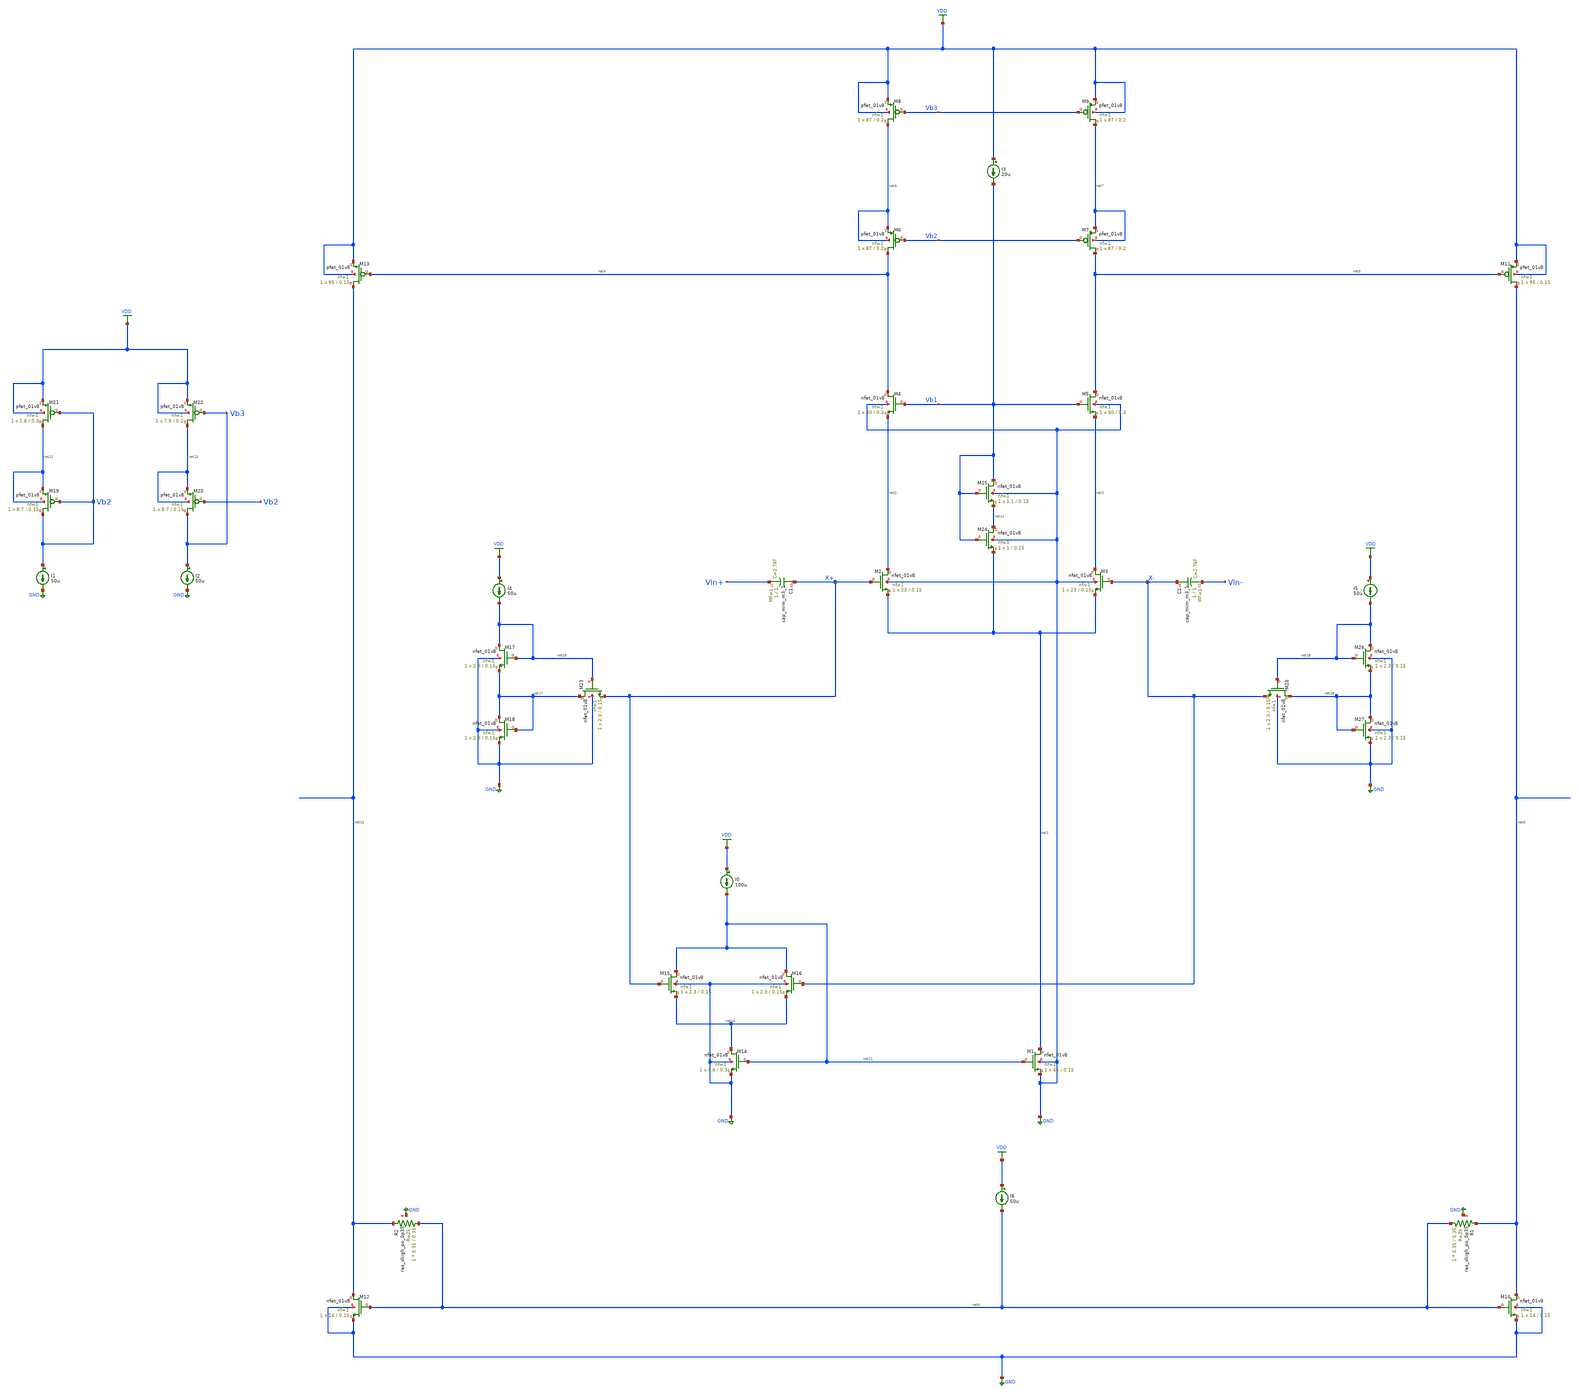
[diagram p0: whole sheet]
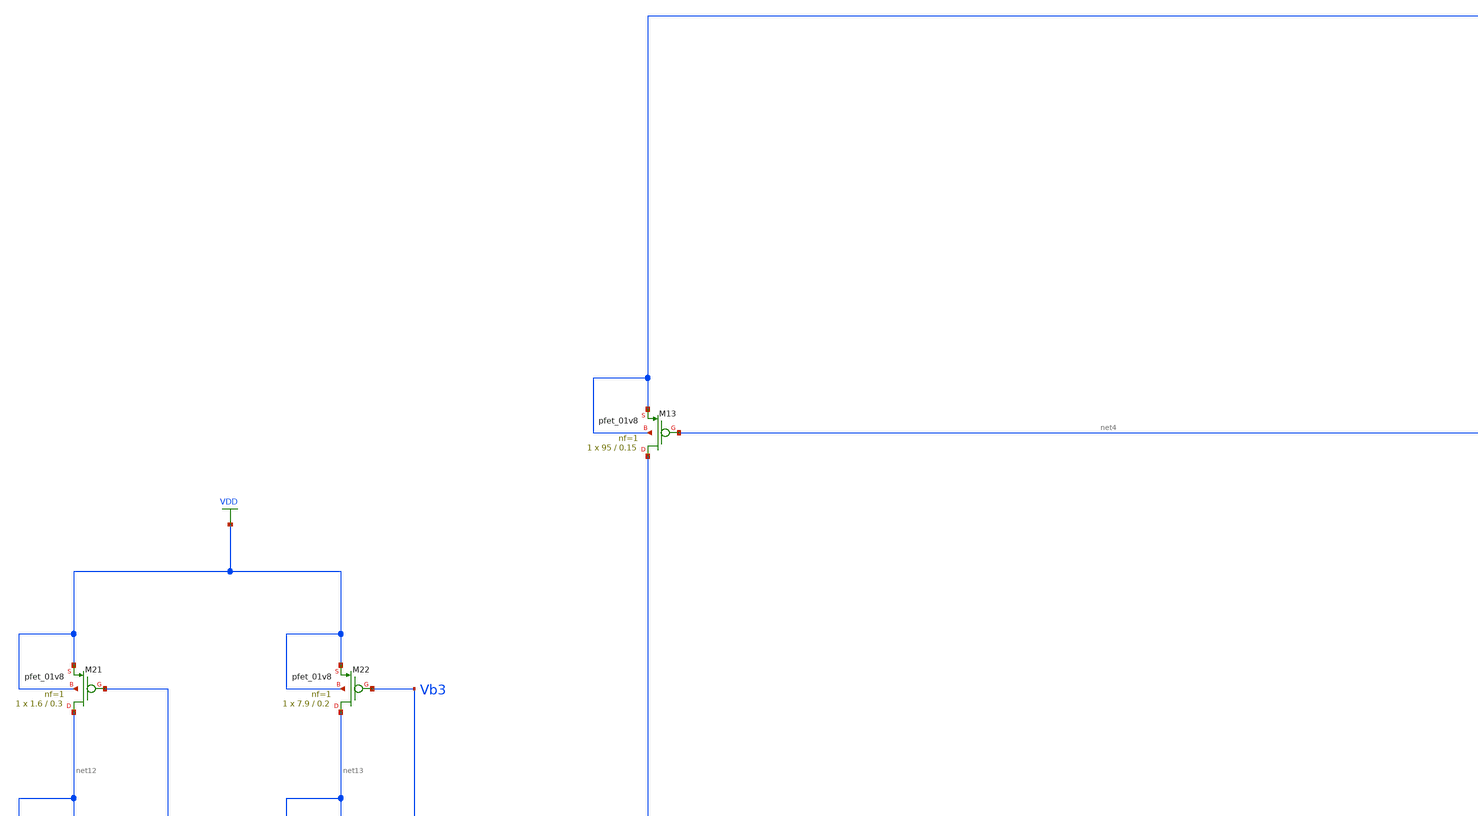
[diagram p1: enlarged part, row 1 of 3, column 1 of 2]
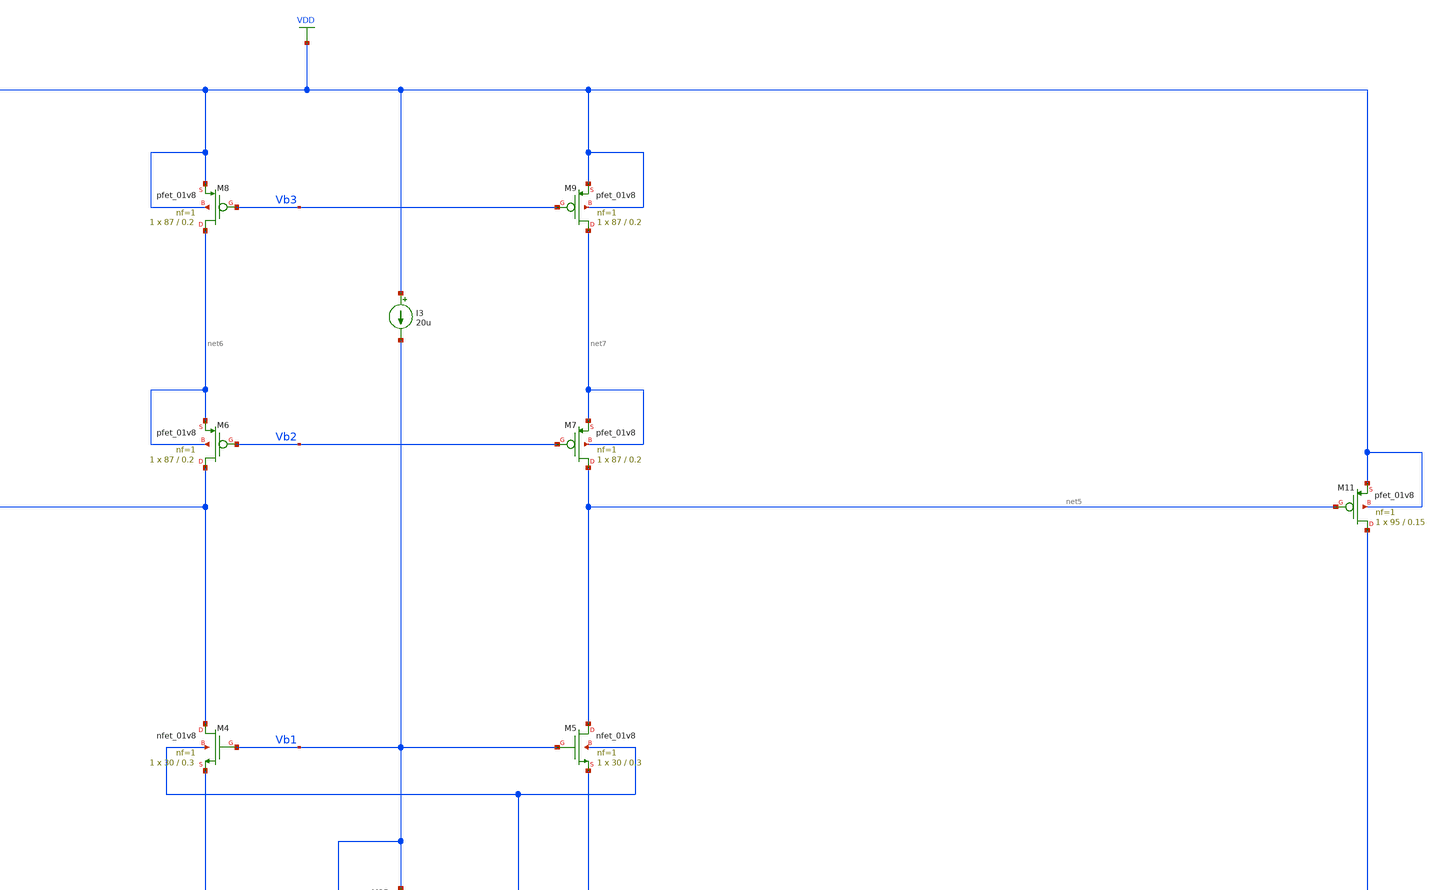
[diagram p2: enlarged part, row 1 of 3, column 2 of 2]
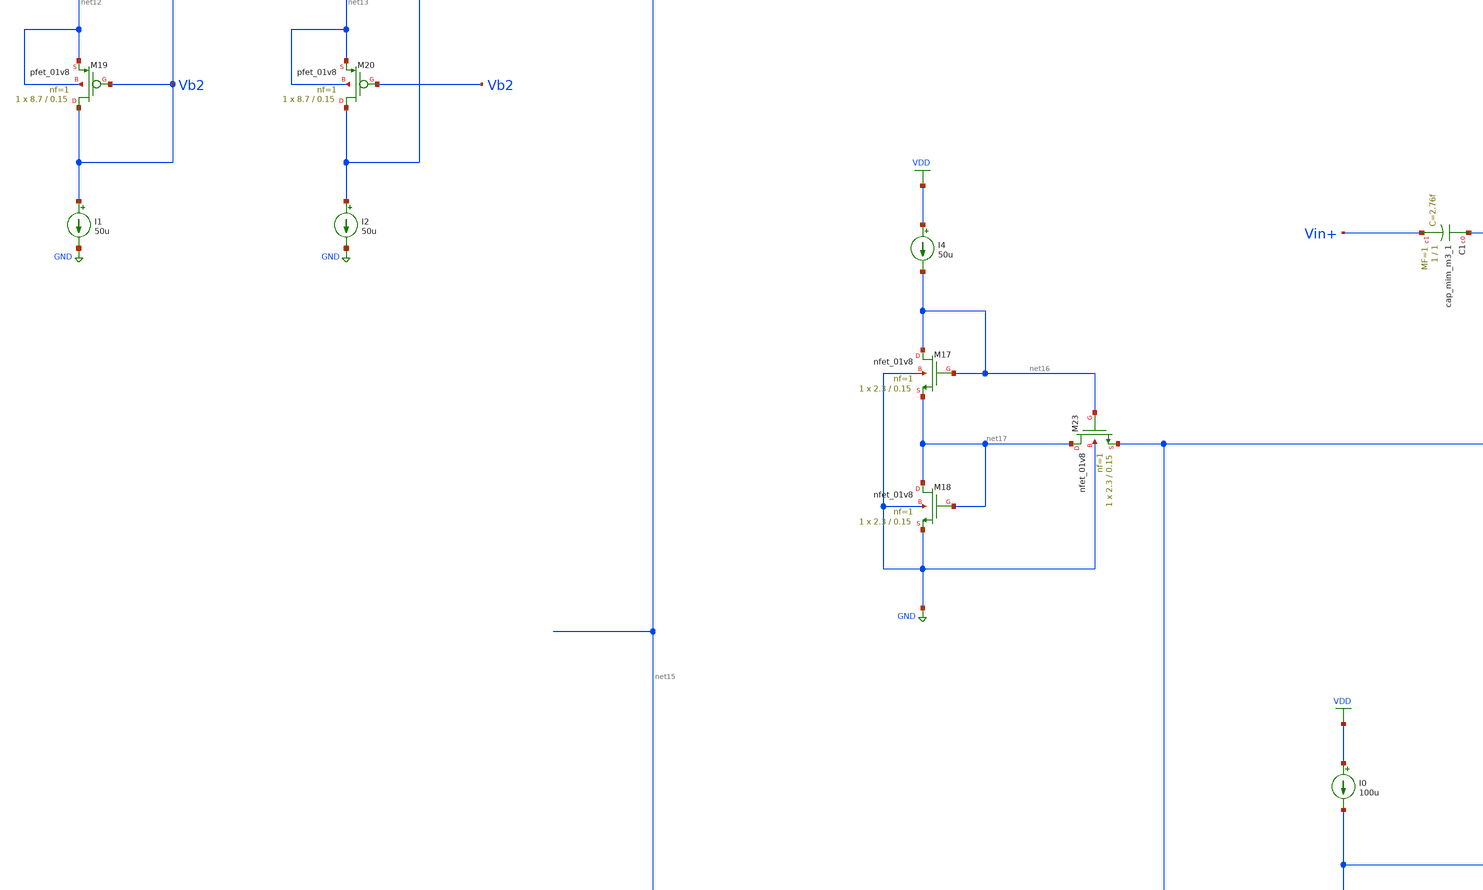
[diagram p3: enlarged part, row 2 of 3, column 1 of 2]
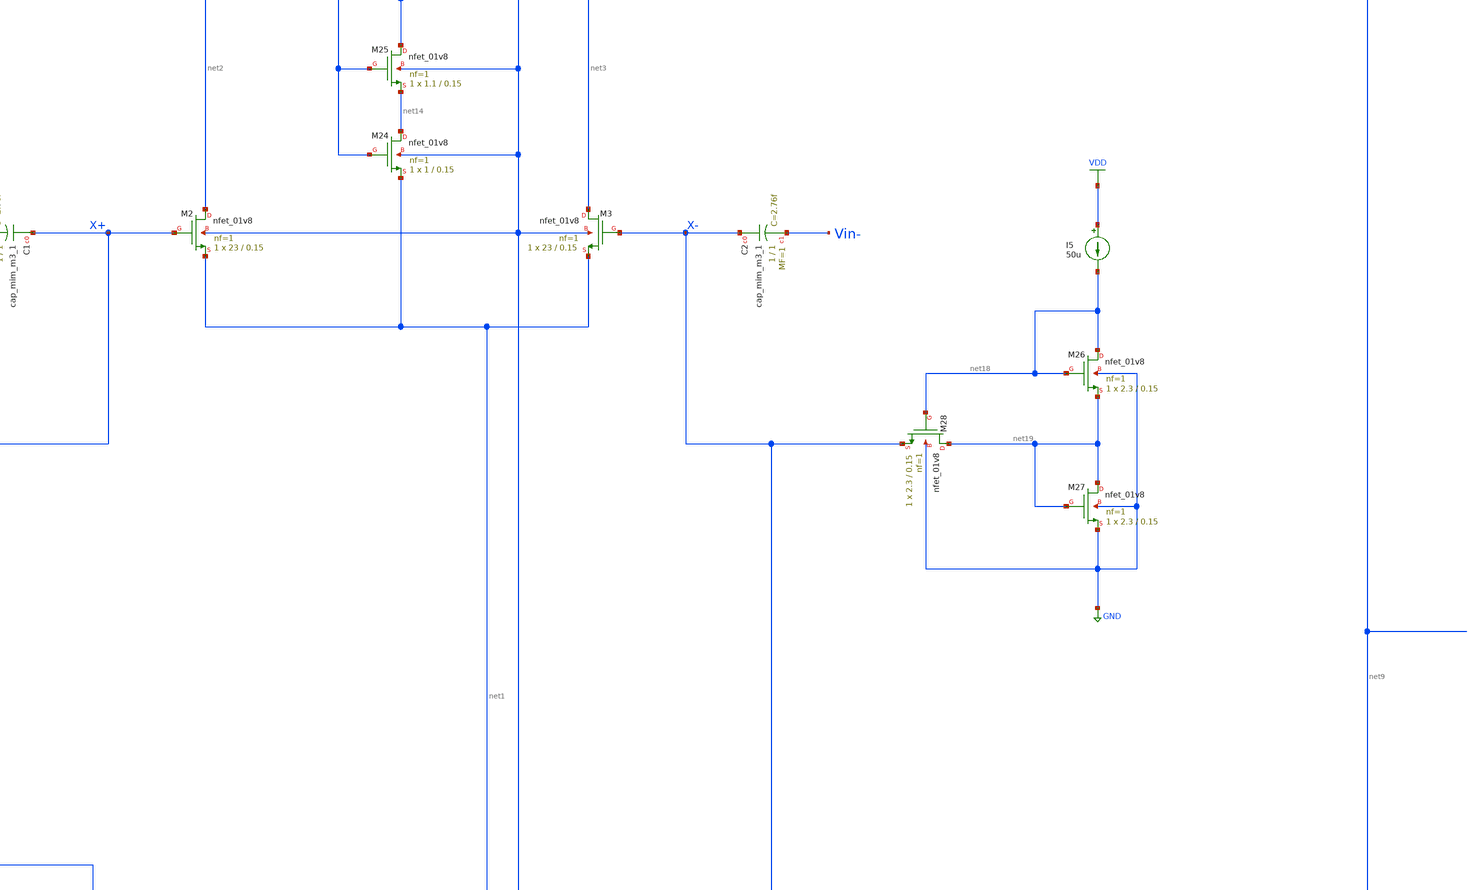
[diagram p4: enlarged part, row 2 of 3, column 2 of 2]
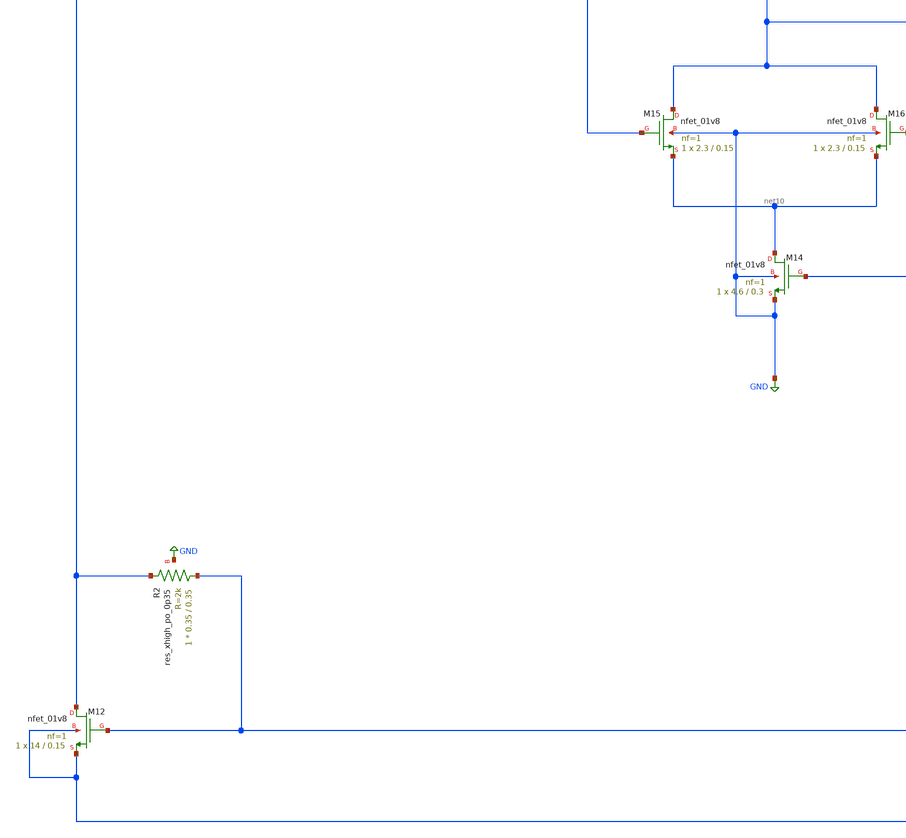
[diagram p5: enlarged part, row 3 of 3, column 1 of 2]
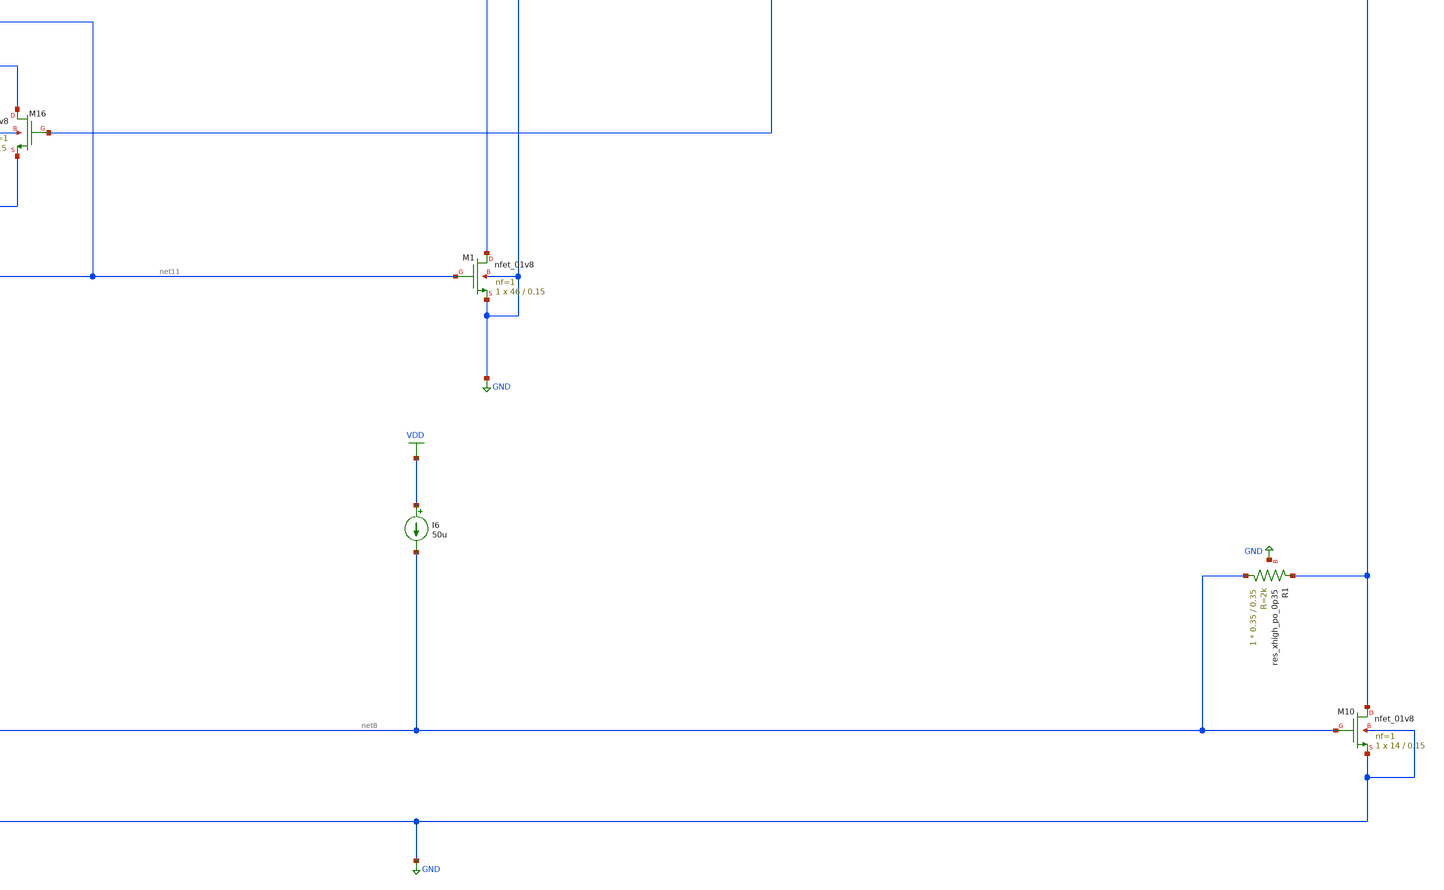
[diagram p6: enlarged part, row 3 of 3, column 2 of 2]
** sch_path: projects/opamp/xschem_ngspice/opamp.sch
**.subckt opamp
XM1 net1 net11 GND GND sky130_fd_pr__nfet_01v8 L=0.15 W=46 nf=1 ad='int((nf+1)/2) * W/nf * 0.29' as='int((nf+2)/2) * W/nf * 0.29'
+ pd='2*int((nf+1)/2) * (W/nf + 0.29)' ps='2*int((nf+2)/2) * (W/nf + 0.29)' nrd='0.29 / W' nrs='0.29 / W'
+ sa=0 sb=0 sd=0 mult=1 m=1
XM2 net2 X+ net1 GND sky130_fd_pr__nfet_01v8 L=0.15 W=23 nf=1 ad='int((nf+1)/2) * W/nf * 0.29' as='int((nf+2)/2) * W/nf * 0.29'
+ pd='2*int((nf+1)/2) * (W/nf + 0.29)' ps='2*int((nf+2)/2) * (W/nf + 0.29)' nrd='0.29 / W' nrs='0.29 / W'
+ sa=0 sb=0 sd=0 mult=1 m=1
XM3 net3 X- net1 GND sky130_fd_pr__nfet_01v8 L=0.15 W=23 nf=1 ad='int((nf+1)/2) * W/nf * 0.29' as='int((nf+2)/2) * W/nf * 0.29'
+ pd='2*int((nf+1)/2) * (W/nf + 0.29)' ps='2*int((nf+2)/2) * (W/nf + 0.29)' nrd='0.29 / W' nrs='0.29 / W'
+ sa=0 sb=0 sd=0 mult=1 m=1
XM4 net4 Vb1 net2 GND sky130_fd_pr__nfet_01v8 L=0.3 W=30 nf=1 ad='int((nf+1)/2) * W/nf * 0.29' as='int((nf+2)/2) * W/nf * 0.29'
+ pd='2*int((nf+1)/2) * (W/nf + 0.29)' ps='2*int((nf+2)/2) * (W/nf + 0.29)' nrd='0.29 / W' nrs='0.29 / W'
+ sa=0 sb=0 sd=0 mult=1 m=1
XM5 net5 Vb1 net3 GND sky130_fd_pr__nfet_01v8 L=0.3 W=30 nf=1 ad='int((nf+1)/2) * W/nf * 0.29' as='int((nf+2)/2) * W/nf * 0.29'
+ pd='2*int((nf+1)/2) * (W/nf + 0.29)' ps='2*int((nf+2)/2) * (W/nf + 0.29)' nrd='0.29 / W' nrs='0.29 / W'
+ sa=0 sb=0 sd=0 mult=1 m=1
XM6 net4 Vb2 net6 net6 sky130_fd_pr__pfet_01v8 L=0.2 W=87 nf=1 ad='int((nf+1)/2) * W/nf * 0.29' as='int((nf+2)/2) * W/nf * 0.29'
+ pd='2*int((nf+1)/2) * (W/nf + 0.29)' ps='2*int((nf+2)/2) * (W/nf + 0.29)' nrd='0.29 / W' nrs='0.29 / W'
+ sa=0 sb=0 sd=0 mult=1 m=1
XM7 net5 Vb2 net7 net7 sky130_fd_pr__pfet_01v8 L=0.2 W=87 nf=1 ad='int((nf+1)/2) * W/nf * 0.29' as='int((nf+2)/2) * W/nf * 0.29'
+ pd='2*int((nf+1)/2) * (W/nf + 0.29)' ps='2*int((nf+2)/2) * (W/nf + 0.29)' nrd='0.29 / W' nrs='0.29 / W'
+ sa=0 sb=0 sd=0 mult=1 m=1
XM8 net6 Vb3 VDD VDD sky130_fd_pr__pfet_01v8 L=0.2 W=87 nf=1 ad='int((nf+1)/2) * W/nf * 0.29' as='int((nf+2)/2) * W/nf * 0.29'
+ pd='2*int((nf+1)/2) * (W/nf + 0.29)' ps='2*int((nf+2)/2) * (W/nf + 0.29)' nrd='0.29 / W' nrs='0.29 / W'
+ sa=0 sb=0 sd=0 mult=1 m=1
XM9 net7 Vb3 VDD VDD sky130_fd_pr__pfet_01v8 L=0.2 W=87 nf=1 ad='int((nf+1)/2) * W/nf * 0.29' as='int((nf+2)/2) * W/nf * 0.29'
+ pd='2*int((nf+1)/2) * (W/nf + 0.29)' ps='2*int((nf+2)/2) * (W/nf + 0.29)' nrd='0.29 / W' nrs='0.29 / W'
+ sa=0 sb=0 sd=0 mult=1 m=1
XM10 net9 net8 GND GND sky130_fd_pr__nfet_01v8 L=0.15 W=14 nf=1 ad='int((nf+1)/2) * W/nf * 0.29' as='int((nf+2)/2) * W/nf * 0.29'
+ pd='2*int((nf+1)/2) * (W/nf + 0.29)' ps='2*int((nf+2)/2) * (W/nf + 0.29)' nrd='0.29 / W' nrs='0.29 / W'
+ sa=0 sb=0 sd=0 mult=1 m=1
XM11 net9 net5 VDD VDD sky130_fd_pr__pfet_01v8 L=0.15 W=95 nf=1 ad='int((nf+1)/2) * W/nf * 0.29' as='int((nf+2)/2) * W/nf * 0.29'
+ pd='2*int((nf+1)/2) * (W/nf + 0.29)' ps='2*int((nf+2)/2) * (W/nf + 0.29)' nrd='0.29 / W' nrs='0.29 / W'
+ sa=0 sb=0 sd=0 mult=1 m=1
XM12 net15 net8 GND GND sky130_fd_pr__nfet_01v8 L=0.15 W=14 nf=1 ad='int((nf+1)/2) * W/nf * 0.29' as='int((nf+2)/2) * W/nf * 0.29'
+ pd='2*int((nf+1)/2) * (W/nf + 0.29)' ps='2*int((nf+2)/2) * (W/nf + 0.29)' nrd='0.29 / W' nrs='0.29 / W'
+ sa=0 sb=0 sd=0 mult=1 m=1
XM13 net15 net4 VDD VDD sky130_fd_pr__pfet_01v8 L=0.15 W=95 nf=1 ad='int((nf+1)/2) * W/nf * 0.29' as='int((nf+2)/2) * W/nf * 0.29'
+ pd='2*int((nf+1)/2) * (W/nf + 0.29)' ps='2*int((nf+2)/2) * (W/nf + 0.29)' nrd='0.29 / W' nrs='0.29 / W'
+ sa=0 sb=0 sd=0 mult=1 m=1
XM14 net10 net11 GND GND sky130_fd_pr__nfet_01v8 L=0.3 W=4.6 nf=1 ad='int((nf+1)/2) * W/nf * 0.29' as='int((nf+2)/2) * W/nf * 0.29'
+ pd='2*int((nf+1)/2) * (W/nf + 0.29)' ps='2*int((nf+2)/2) * (W/nf + 0.29)' nrd='0.29 / W' nrs='0.29 / W'
+ sa=0 sb=0 sd=0 mult=1 m=1
XM15 net11 X+ net10 GND sky130_fd_pr__nfet_01v8 L=0.15 W=2.3 nf=1 ad='int((nf+1)/2) * W/nf * 0.29' as='int((nf+2)/2) * W/nf * 0.29'
+ pd='2*int((nf+1)/2) * (W/nf + 0.29)' ps='2*int((nf+2)/2) * (W/nf + 0.29)' nrd='0.29 / W' nrs='0.29 / W'
+ sa=0 sb=0 sd=0 mult=1 m=1
XM16 net11 X- net10 GND sky130_fd_pr__nfet_01v8 L=0.15 W=2.3 nf=1 ad='int((nf+1)/2) * W/nf * 0.29' as='int((nf+2)/2) * W/nf * 0.29'
+ pd='2*int((nf+1)/2) * (W/nf + 0.29)' ps='2*int((nf+2)/2) * (W/nf + 0.29)' nrd='0.29 / W' nrs='0.29 / W'
+ sa=0 sb=0 sd=0 mult=1 m=1
XM19 Vb2 Vb2 net12 net12 sky130_fd_pr__pfet_01v8 L=0.15 W=8.7 nf=1 ad='int((nf+1)/2) * W/nf * 0.29' as='int((nf+2)/2) * W/nf * 0.29'
+ pd='2*int((nf+1)/2) * (W/nf + 0.29)' ps='2*int((nf+2)/2) * (W/nf + 0.29)' nrd='0.29 / W' nrs='0.29 / W'
+ sa=0 sb=0 sd=0 mult=1 m=1
XM20 Vb3 Vb2 net13 net13 sky130_fd_pr__pfet_01v8 L=0.15 W=8.7 nf=1 ad='int((nf+1)/2) * W/nf * 0.29' as='int((nf+2)/2) * W/nf * 0.29'
+ pd='2*int((nf+1)/2) * (W/nf + 0.29)' ps='2*int((nf+2)/2) * (W/nf + 0.29)' nrd='0.29 / W' nrs='0.29 / W'
+ sa=0 sb=0 sd=0 mult=1 m=1
XM21 net12 Vb2 VDD VDD sky130_fd_pr__pfet_01v8 L=0.3 W=1.6 nf=1 ad='int((nf+1)/2) * W/nf * 0.29' as='int((nf+2)/2) * W/nf * 0.29'
+ pd='2*int((nf+1)/2) * (W/nf + 0.29)' ps='2*int((nf+2)/2) * (W/nf + 0.29)' nrd='0.29 / W' nrs='0.29 / W'
+ sa=0 sb=0 sd=0 mult=1 m=1
XM22 net13 Vb3 VDD VDD sky130_fd_pr__pfet_01v8 L=0.2 W=7.9 nf=1 ad='int((nf+1)/2) * W/nf * 0.29' as='int((nf+2)/2) * W/nf * 0.29'
+ pd='2*int((nf+1)/2) * (W/nf + 0.29)' ps='2*int((nf+2)/2) * (W/nf + 0.29)' nrd='0.29 / W' nrs='0.29 / W'
+ sa=0 sb=0 sd=0 mult=1 m=1
XM24 net14 Vb1 net1 GND sky130_fd_pr__nfet_01v8 L=0.15 W=1 nf=1 ad='int((nf+1)/2) * W/nf * 0.29' as='int((nf+2)/2) * W/nf * 0.29'
+ pd='2*int((nf+1)/2) * (W/nf + 0.29)' ps='2*int((nf+2)/2) * (W/nf + 0.29)' nrd='0.29 / W' nrs='0.29 / W'
+ sa=0 sb=0 sd=0 mult=1 m=1
XM25 Vb1 Vb1 net14 GND sky130_fd_pr__nfet_01v8 L=0.15 W=1.1 nf=1 ad='int((nf+1)/2) * W/nf * 0.29' as='int((nf+2)/2) * W/nf * 0.29'
+ pd='2*int((nf+1)/2) * (W/nf + 0.29)' ps='2*int((nf+2)/2) * (W/nf + 0.29)' nrd='0.29 / W' nrs='0.29 / W'
+ sa=0 sb=0 sd=0 mult=1 m=1
I0 VDD net11 100u
I1 Vb2 GND 50u
I2 Vb3 GND 50u
I3 VDD Vb1 20u
I4 VDD net16 50u
XM17 net16 net16 net17 GND sky130_fd_pr__nfet_01v8 L=0.15 W=2.3 nf=1 ad='int((nf+1)/2) * W/nf * 0.29'
+ as='int((nf+2)/2) * W/nf * 0.29' pd='2*int((nf+1)/2) * (W/nf + 0.29)' ps='2*int((nf+2)/2) * (W/nf + 0.29)'
+ nrd='0.29 / W' nrs='0.29 / W' sa=0 sb=0 sd=0 mult=1 m=1
XM18 net17 net17 GND GND sky130_fd_pr__nfet_01v8 L=0.15 W=2.3 nf=1 ad='int((nf+1)/2) * W/nf * 0.29' as='int((nf+2)/2) * W/nf * 0.29'
+ pd='2*int((nf+1)/2) * (W/nf + 0.29)' ps='2*int((nf+2)/2) * (W/nf + 0.29)' nrd='0.29 / W' nrs='0.29 / W'
+ sa=0 sb=0 sd=0 mult=1 m=1
XM23 net17 net16 X+ GND sky130_fd_pr__nfet_01v8 L=0.15 W=2.3 nf=1 ad='int((nf+1)/2) * W/nf * 0.29' as='int((nf+2)/2) * W/nf * 0.29'
+ pd='2*int((nf+1)/2) * (W/nf + 0.29)' ps='2*int((nf+2)/2) * (W/nf + 0.29)' nrd='0.29 / W' nrs='0.29 / W'
+ sa=0 sb=0 sd=0 mult=1 m=1
XC1 X+ Vin+ sky130_fd_pr__cap_mim_m3_1 W=1 L=1 MF=1 m=1
I5 VDD net18 50u
XM26 net18 net18 net19 GND sky130_fd_pr__nfet_01v8 L=0.15 W=2.3 nf=1 ad='int((nf+1)/2) * W/nf * 0.29'
+ as='int((nf+2)/2) * W/nf * 0.29' pd='2*int((nf+1)/2) * (W/nf + 0.29)' ps='2*int((nf+2)/2) * (W/nf + 0.29)'
+ nrd='0.29 / W' nrs='0.29 / W' sa=0 sb=0 sd=0 mult=1 m=1
XM27 net19 net19 GND GND sky130_fd_pr__nfet_01v8 L=0.15 W=2.3 nf=1 ad='int((nf+1)/2) * W/nf * 0.29' as='int((nf+2)/2) * W/nf * 0.29'
+ pd='2*int((nf+1)/2) * (W/nf + 0.29)' ps='2*int((nf+2)/2) * (W/nf + 0.29)' nrd='0.29 / W' nrs='0.29 / W'
+ sa=0 sb=0 sd=0 mult=1 m=1
XM28 net19 net18 X- GND sky130_fd_pr__nfet_01v8 L=0.15 W=2.3 nf=1 ad='int((nf+1)/2) * W/nf * 0.29' as='int((nf+2)/2) * W/nf * 0.29'
+ pd='2*int((nf+1)/2) * (W/nf + 0.29)' ps='2*int((nf+2)/2) * (W/nf + 0.29)' nrd='0.29 / W' nrs='0.29 / W'
+ sa=0 sb=0 sd=0 mult=1 m=1
XC2 X- Vin- sky130_fd_pr__cap_mim_m3_1 W=1 L=1 MF=1 m=1
XR1 net8 net9 GND sky130_fd_pr__res_xhigh_po_0p35 L=0.35 mult=1 m=1
XR2 net8 net15 GND sky130_fd_pr__res_xhigh_po_0p35 L=0.35 mult=1 m=1
I6 VDD net8 50u
**.ends
.GLOBAL VDD
.GLOBAL GND
.end
